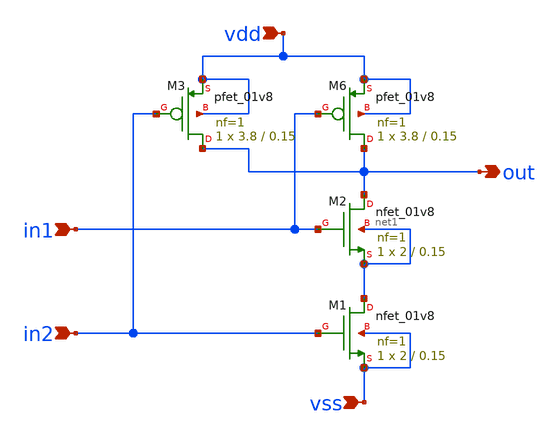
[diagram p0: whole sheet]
** sch_path: projects/carry_lookahead_adder/xschem/ports/nand.sch
**.subckt nand in1 in2 vdd vss out
*.ipin in1
*.ipin in2
*.ipin vdd
*.ipin vss
*.opin out
XM1 net1 in2 vss vss sky130_fd_pr__nfet_01v8 L=0.15 W=2 nf=1 ad='int((nf+1)/2) * W/nf * 0.29' as='int((nf+2)/2) * W/nf * 0.29'
+ pd='2*int((nf+1)/2) * (W/nf + 0.29)' ps='2*int((nf+2)/2) * (W/nf + 0.29)' nrd='0.29 / W' nrs='0.29 / W'
+ sa=0 sb=0 sd=0 mult=1 m=1
XM2 out in1 net1 net1 sky130_fd_pr__nfet_01v8 L=0.15 W=2 nf=1 ad='int((nf+1)/2) * W/nf * 0.29' as='int((nf+2)/2) * W/nf * 0.29'
+ pd='2*int((nf+1)/2) * (W/nf + 0.29)' ps='2*int((nf+2)/2) * (W/nf + 0.29)' nrd='0.29 / W' nrs='0.29 / W'
+ sa=0 sb=0 sd=0 mult=1 m=1
XM6 out in1 vdd vdd sky130_fd_pr__pfet_01v8 L=0.15 W=3.8 nf=1 ad='int((nf+1)/2) * W/nf * 0.29' as='int((nf+2)/2) * W/nf * 0.29'
+ pd='2*int((nf+1)/2) * (W/nf + 0.29)' ps='2*int((nf+2)/2) * (W/nf + 0.29)' nrd='0.29 / W' nrs='0.29 / W'
+ sa=0 sb=0 sd=0 mult=1 m=1
XM3 out in2 vdd vdd sky130_fd_pr__pfet_01v8 L=0.15 W=3.8 nf=1 ad='int((nf+1)/2) * W/nf * 0.29' as='int((nf+2)/2) * W/nf * 0.29'
+ pd='2*int((nf+1)/2) * (W/nf + 0.29)' ps='2*int((nf+2)/2) * (W/nf + 0.29)' nrd='0.29 / W' nrs='0.29 / W'
+ sa=0 sb=0 sd=0 mult=1 m=1
**.ends
.end
